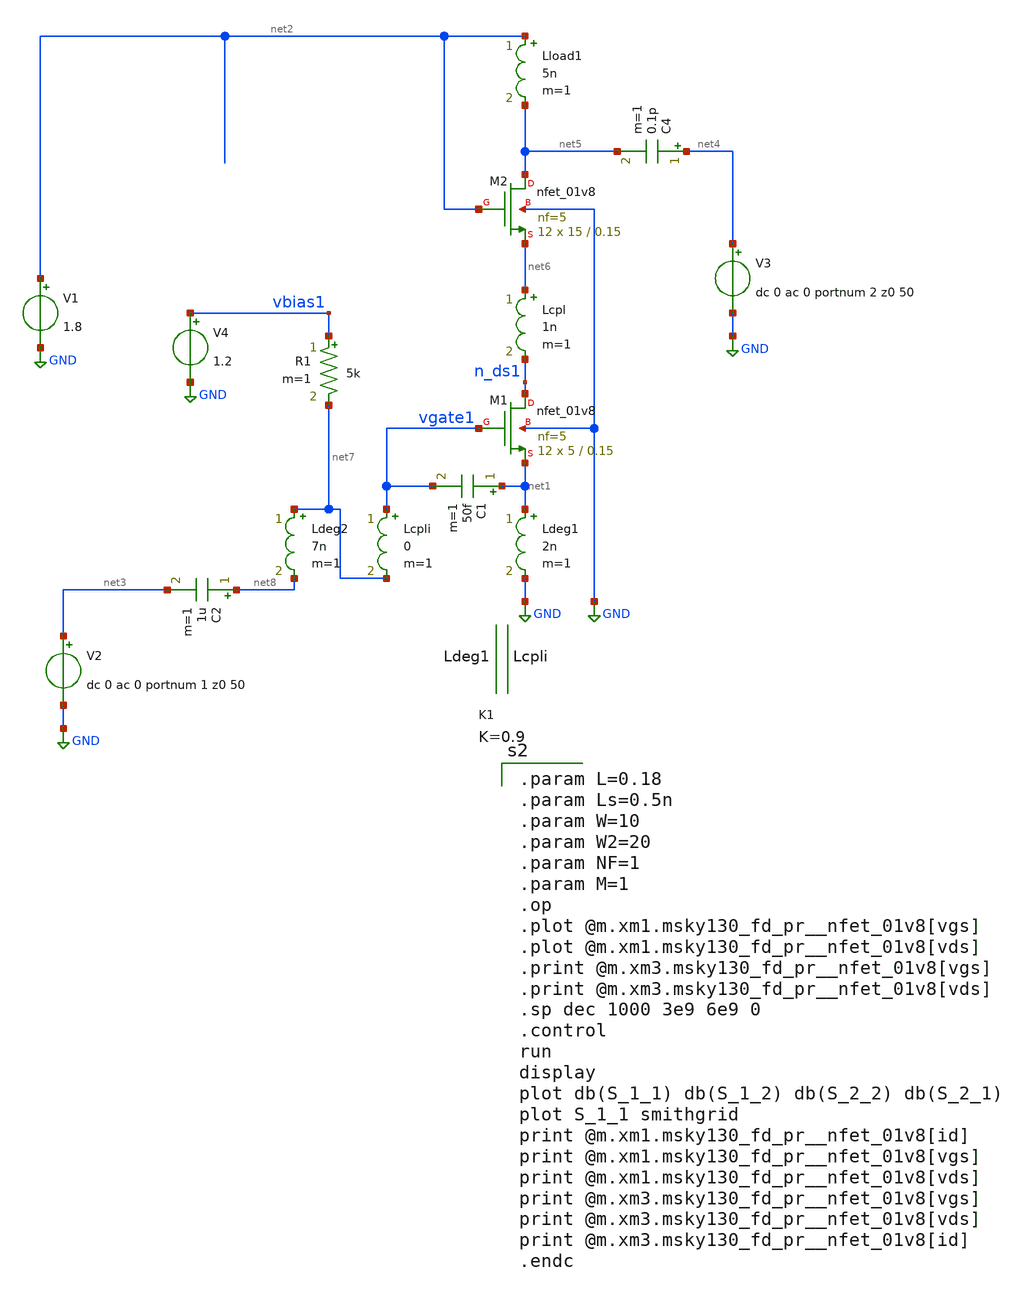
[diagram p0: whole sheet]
** sch_path: xschem/LNA24_2.sch
**.subckt LNA24_2
XM1 n_ds1 vgate1 net1 GND sky130_fd_pr__nfet_01v8 L=0.15 W=5 nf=5 ad='int((nf+1)/2) * W/nf * 0.29' as='int((nf+2)/2) * W/nf * 0.29'
+ pd='2*int((nf+1)/2) * (W/nf + 0.29)' ps='2*int((nf+2)/2) * (W/nf + 0.29)' nrd='0.29 / W' nrs='0.29 / W'
+ sa=0 sb=0 sd=0 mult=12 m=12
Ldeg1 net1 GND 2n m=1
V1 net2 GND 1.8
V2 net3 GND dc 0 ac 0 portnum 1 z0 50
C2 net8 net3 1u m=1
V3 net4 GND dc 0 ac 0 portnum 2 z0 50
C4 net4 net5 0.1p m=1
Ldeg2 net7 net8 7n m=1
R1 vbias1 net7 5k m=1
Lload1 net2 net5 5n m=1
V4 vbias1 GND 1.2
XM2 net5 net2 net6 GND sky130_fd_pr__nfet_01v8 L=0.15 W=15 nf=5 ad='int((nf+1)/2) * W/nf * 0.29' as='int((nf+2)/2) * W/nf * 0.29'
+ pd='2*int((nf+1)/2) * (W/nf + 0.29)' ps='2*int((nf+2)/2) * (W/nf + 0.29)' nrd='0.29 / W' nrs='0.29 / W'
+ sa=0 sb=0 sd=0 mult=12 m=12
Lcpl net6 n_ds1 1n m=1
K1 Ldeg1 Lcpli 0.9
Lcpli vgate1 net7 0 m=1
C1 net1 vgate1 50f m=1
**** begin user architecture code
.lib $::SKYWATER_MODELS/sky130.lib.spice tt
.include $::PDKPATH/libs.ref/sky130_fd_sc_hvl/spice/sky130_fd_sc_hvl.spice

.param L=0.18
.param Ls=0.5n
.param W=10
.param W2=20
.param NF=1
.param M=1
.op
.plot @m.xm1.msky130_fd_pr__nfet_01v8[vgs]
.plot @m.xm1.msky130_fd_pr__nfet_01v8[vds]
.print @m.xm3.msky130_fd_pr__nfet_01v8[vgs]
.print @m.xm3.msky130_fd_pr__nfet_01v8[vds]
.sp dec 1000 3e9 6e9 0
.control
run
display
plot db(S_1_1) db(S_1_2) db(S_2_2) db(S_2_1)
plot S_1_1 smithgrid
print @m.xm1.msky130_fd_pr__nfet_01v8[id]
print @m.xm1.msky130_fd_pr__nfet_01v8[vgs]
print @m.xm1.msky130_fd_pr__nfet_01v8[vds]
print @m.xm3.msky130_fd_pr__nfet_01v8[vgs]
print @m.xm3.msky130_fd_pr__nfet_01v8[vds]
print @m.xm3.msky130_fd_pr__nfet_01v8[id]
.endc


**** end user architecture code
**.ends
.GLOBAL GND
.end
